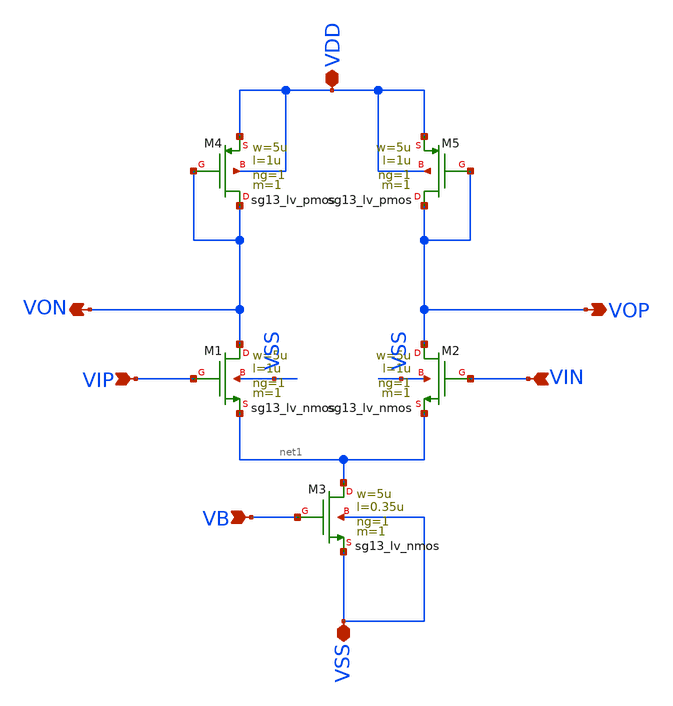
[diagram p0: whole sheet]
** sch_path: BTDay4-Ex/diff_diode_load.sch
**.subckt diff_diode_load VIN VIP VON VOP VB VDD VSS
*.ipin VIN
*.ipin VIP
*.opin VON
*.opin VOP
*.ipin VB
*.iopin VDD
*.iopin VSS
XM1 VON VIP net1 VSS sg13_lv_nmos w=5u l=1u ng=1 m=1 mm_ok=1
XM2 VOP VIN net1 VSS sg13_lv_nmos w=5u l=1u ng=1 m=1 mm_ok=1
XM3 net1 VB VSS VSS sg13_lv_nmos w=5u l=0.35u ng=1 m=1 mm_ok=1
XM4 VON VON VDD VDD sg13_lv_pmos w=5u l=1u ng=1 m=1 mm_ok=1
XM5 VOP VOP VDD VDD sg13_lv_pmos w=5u l=1u ng=1 m=1 mm_ok=1
**.ends
.end
